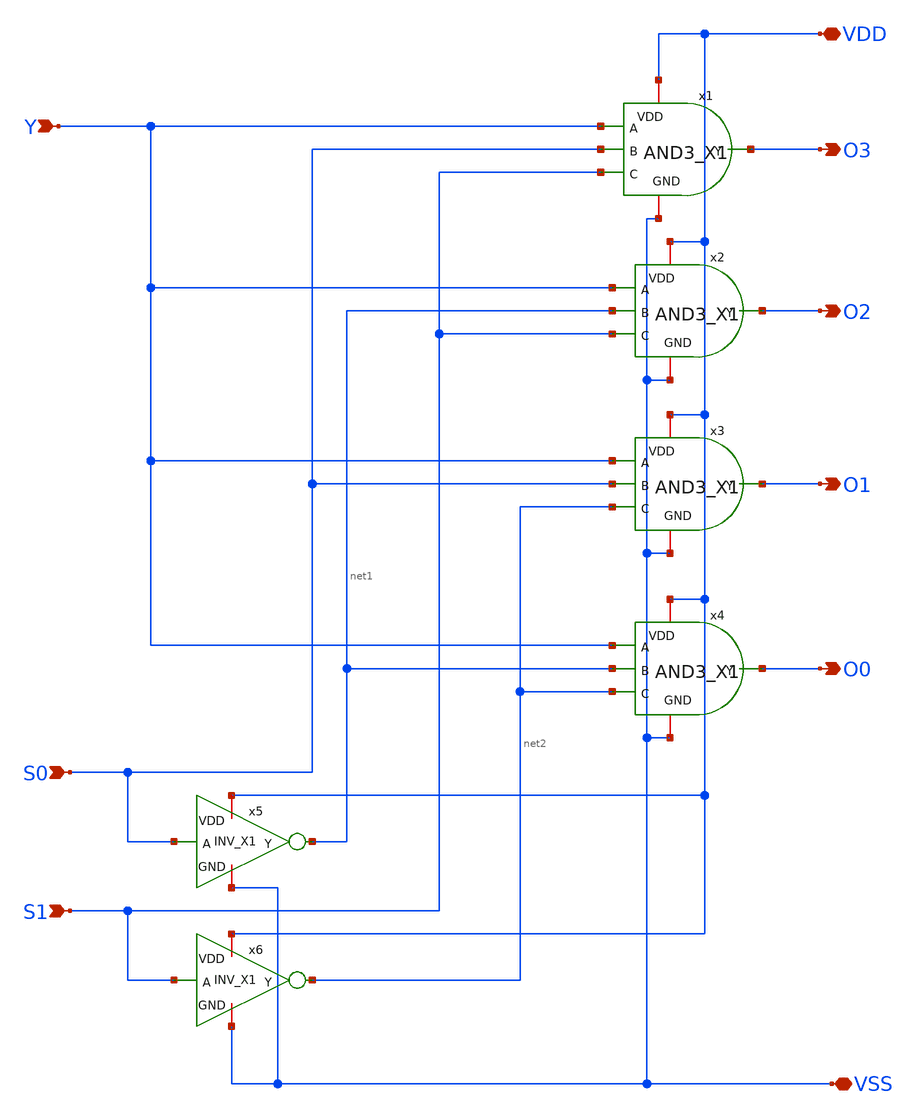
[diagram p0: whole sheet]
** sch_path: MUX/DEMUX4.sch
**.subckt DEMUX4 Y S0 S1 O0 O1 O2 O3 VDD VSS
*.ipin Y
*.ipin S0
*.ipin S1
*.opin O0
*.opin O1
*.opin O2
*.opin O3
*.iopin VDD
*.iopin VSS
x1 S1 VDD O3 Y S0 VSS AND3_X1
x2 S1 VDD O2 Y net1 VSS AND3_X1
x3 net2 VDD O1 Y S0 VSS AND3_X1
x4 net2 VDD O0 Y net1 VSS AND3_X1
x5 VDD S0 net1 VSS INV_X1
x6 VDD S1 net2 VSS INV_X1
**.ends

* expanding   symbol:  IP62_5_stdcell/AND3_X1.sym # of pins=6
** sym_path: IP62_5_stdcell/AND3_X1.sym
** sch_path: IP62_5_stdcell/AND3_X1.sch
.subckt AND3_X1 C VDD Y A B GND
*.opin Y
*.ipin A
*.ipin B
*.iopin VDD
*.iopin GND
*.ipin C
XM4 net1 C VDD VDD PMOS w=10.2u l=1u as=0 ad=0 ps=0 pd=0 nrd=0 nrs=0 m=1
XM2 net1 B VDD VDD PMOS w=10.2u l=1u as=0 ad=0 ps=0 pd=0 nrd=0 nrs=0 m=1
XM3 Y net1 VDD VDD PMOS w=10.2u l=1u as=0 ad=0 ps=0 pd=0 nrd=0 nrs=0 m=1
XM1 VDD A net1 VDD PMOS w=10.2u l=1u as=0 ad=0 ps=0 pd=0 nrd=0 nrs=0 m=1
XM8 Y net1 GND GND NMOS w=3.4u l=1u as=0 ad=0 ps=0 pd=0 nrd=0 nrs=0 m=1
XM5 net1 A net3 GND NMOS w=3.4u l=1u as=0 ad=0 ps=0 pd=0 nrd=0 nrs=0 m=1
XM6 net3 B net2 GND NMOS w=3.4u l=1u as=0 ad=0 ps=0 pd=0 nrd=0 nrs=0 m=1
XM7 net2 C GND GND NMOS w=3.4u l=1u as=0 ad=0 ps=0 pd=0 nrd=0 nrs=0 m=1
.ends


* expanding   symbol:  IP62_5_stdcell/INV_X1.sym # of pins=4
** sym_path: IP62_5_stdcell/INV_X1.sym
** sch_path: IP62_5_stdcell/INV_X1.sch
.subckt INV_X1 VDD A Y GND
*.ipin A
*.opin Y
*.iopin GND
*.iopin VDD
XM7 Y A VDD VDD PMOS w=10.2u l=1u as=0 ad=0 ps=0 pd=0 nrd=0 nrs=0 m=1
XM2 Y A GND GND NMOS w=3.4u l=1u as=0 ad=0 ps=0 pd=0 nrd=0 nrs=0 m=1
.ends

.end
